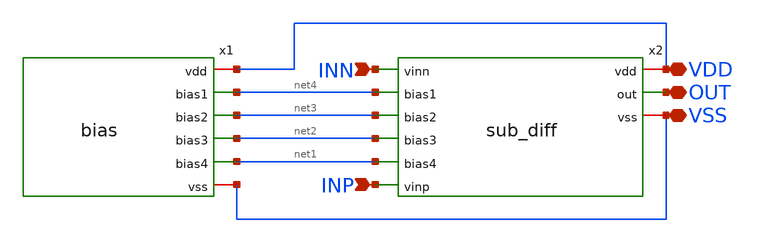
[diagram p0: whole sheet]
** sch_path: FINAL/XSCHEM/OPAM/COMP_sc.sch
**.subckt COMP_sc INN INP VDD VSS OUT
*.ipin INN
*.ipin INP
*.iopin VDD
*.iopin VSS
*.iopin OUT
x1 VDD net4 net3 net2 net1 VSS bias
x2 VDD net4 net3 INN OUT INP net2 net1 VSS sub_diff
**.ends
.end
